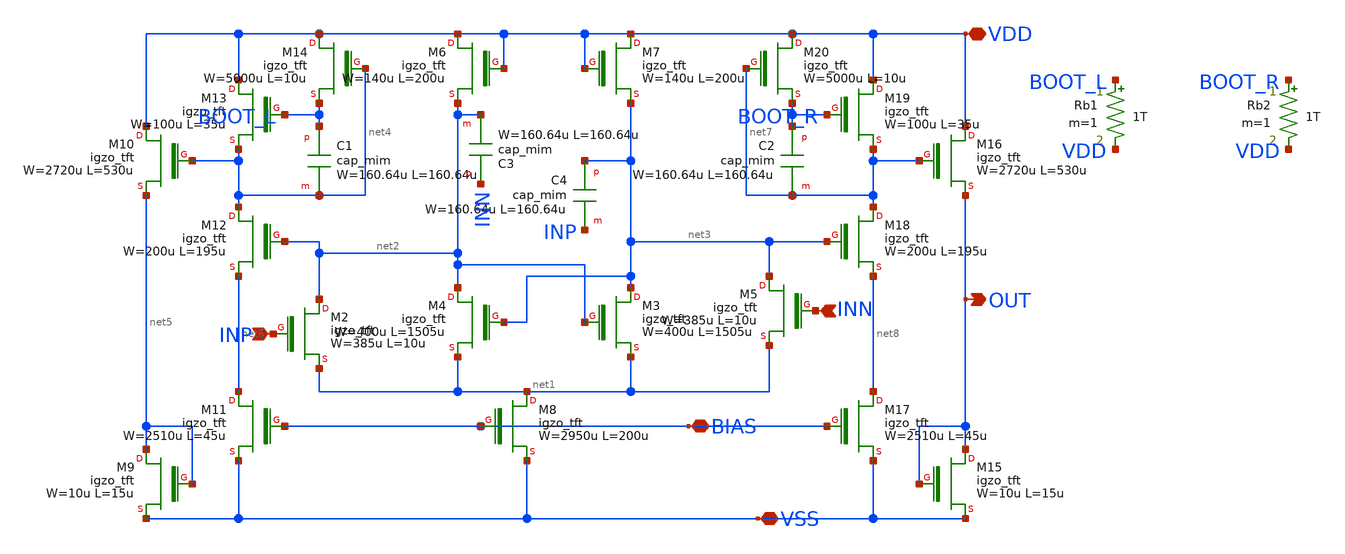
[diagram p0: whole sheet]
** sch_path: OPAM/OPAM.sch
**.subckt OPAM INP VDD INN VSS BIAS OUT
*.ipin INP
*.iopin VDD
*.ipin INN
*.iopin VSS
*.iopin BIAS
*.opin OUT
XM2 net2 INP net1 igzo_tft W=385u L=10u ov=5u nf=1 m=1
XM4 net2 net3 net1 igzo_tft W=400u L=1505u ov=5u nf=1 m=1
XM3 net3 net2 net1 igzo_tft W=400u L=1505u ov=5u nf=1 m=1
XM5 net3 INN net1 igzo_tft W=385u L=10u ov=5u nf=1 m=1
XM6 VDD VDD net2 igzo_tft W=140u L=200u ov=5u nf=1 m=1
XM7 VDD VDD net3 igzo_tft W=140u L=200u ov=5u nf=1 m=1
XM8 net1 BIAS VSS igzo_tft W=2950u L=200u ov=5u nf=1 m=1
XM9 net5 net5 VSS igzo_tft W=10u L=15u ov=5u nf=1 m=1
XM10 VDD net4 net5 igzo_tft W=2720u L=530u ov=5u nf=1 m=1
XM11 net6 BIAS VSS igzo_tft W=2510u L=45u ov=5u nf=1 m=1
XM12 net4 net2 net6 igzo_tft W=200u L=195u ov=5u nf=1 m=1
XM13 VDD BOOT_L net4 igzo_tft W=100u L=35u ov=5u nf=1 m=1
XM14 VDD net4 BOOT_L igzo_tft W=5000u L=10u ov=5u nf=1 m=1
XC1 BOOT_L net4 cap_mim W=160.64u L=160.64u
XM15 OUT OUT VSS igzo_tft W=10u L=15u ov=5u nf=1 m=1
XM16 VDD net7 OUT igzo_tft W=2720u L=530u ov=5u nf=1 m=1
XM17 net8 BIAS VSS igzo_tft W=2510u L=45u ov=5u nf=1 m=1
XM18 net7 net3 net8 igzo_tft W=200u L=195u ov=5u nf=1 m=1
XM19 VDD BOOT_R net7 igzo_tft W=100u L=35u ov=5u nf=1 m=1
XM20 VDD net7 BOOT_R igzo_tft W=5000u L=10u ov=5u nf=1 m=1
XC2 BOOT_R net7 cap_mim W=160.64u L=160.64u
XC3 INN net2 cap_mim W=160.64u L=160.64u
XC4 net3 INP cap_mim W=160.64u L=160.64u
Rb1 BOOT_L VDD 1T m=1
Rb2 BOOT_R VDD 1T m=1
**.ends
.end
